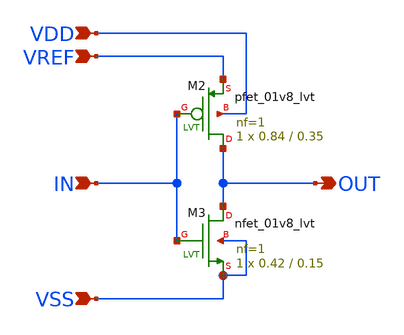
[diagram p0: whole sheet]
** sch_path: hgu/xschem/hgu_inverter.sch
**.subckt hgu_inverter IN VREF VSS OUT VDD
*.ipin IN
*.ipin VREF
*.ipin VSS
*.opin OUT
*.ipin VDD
XM2 OUT IN VREF VDD sky130_fd_pr__pfet_01v8_lvt L=0.35 W=0.84 nf=1 ad='int((nf+1)/2) * W/nf * 0.29' as='int((nf+2)/2) * W/nf * 0.29'
+ pd='2*int((nf+1)/2) * (W/nf + 0.29)' ps='2*int((nf+2)/2) * (W/nf + 0.29)' nrd='0.29 / W' nrs='0.29 / W'
+ sa=0 sb=0 sd=0 mult=1 m=1
XM3 OUT IN VSS VSS sky130_fd_pr__nfet_01v8_lvt L=0.15 W=0.42 nf=1 ad='int((nf+1)/2) * W/nf * 0.29' as='int((nf+2)/2) * W/nf * 0.29'
+ pd='2*int((nf+1)/2) * (W/nf + 0.29)' ps='2*int((nf+2)/2) * (W/nf + 0.29)' nrd='0.29 / W' nrs='0.29 / W'
+ sa=0 sb=0 sd=0 mult=1 m=1
**.ends
.end
